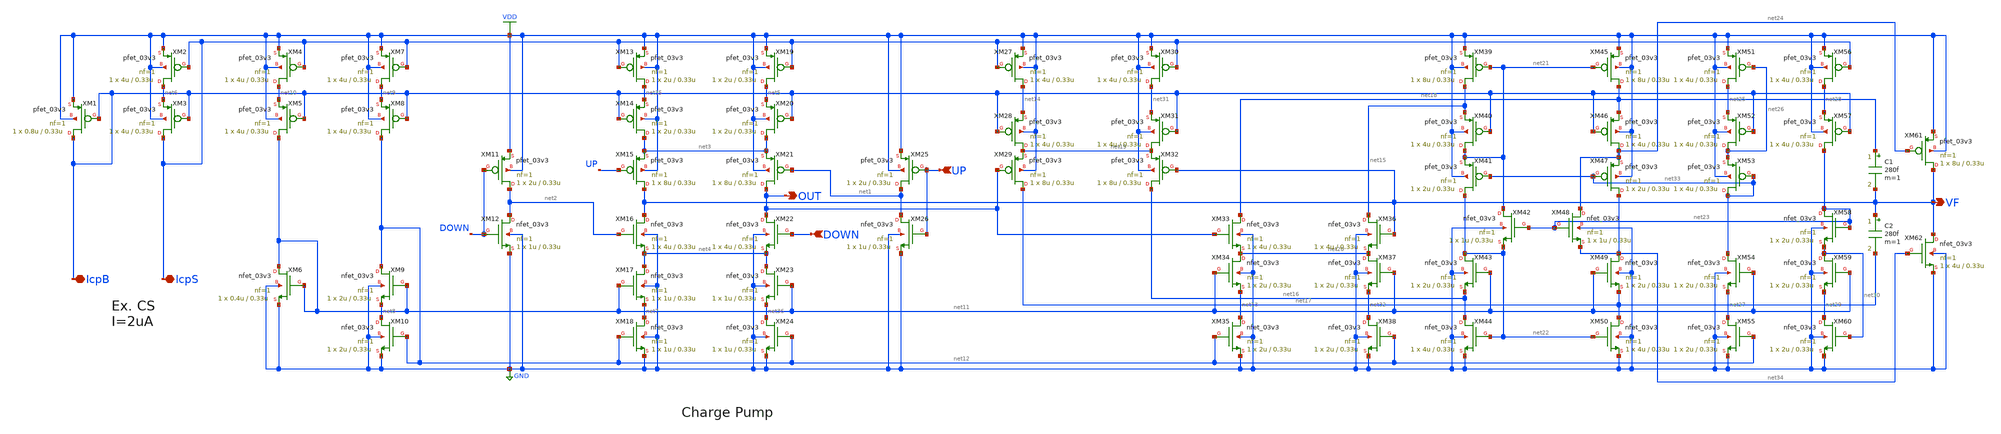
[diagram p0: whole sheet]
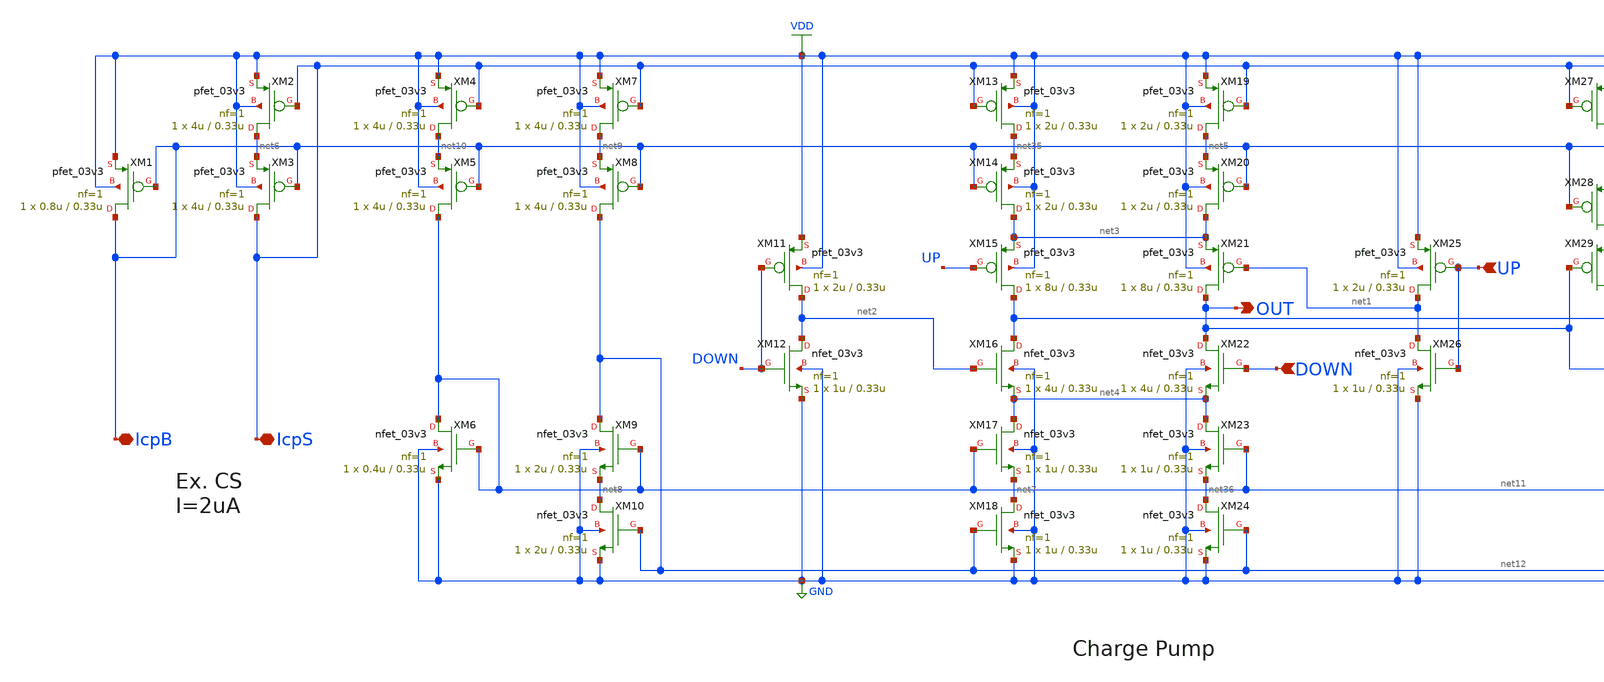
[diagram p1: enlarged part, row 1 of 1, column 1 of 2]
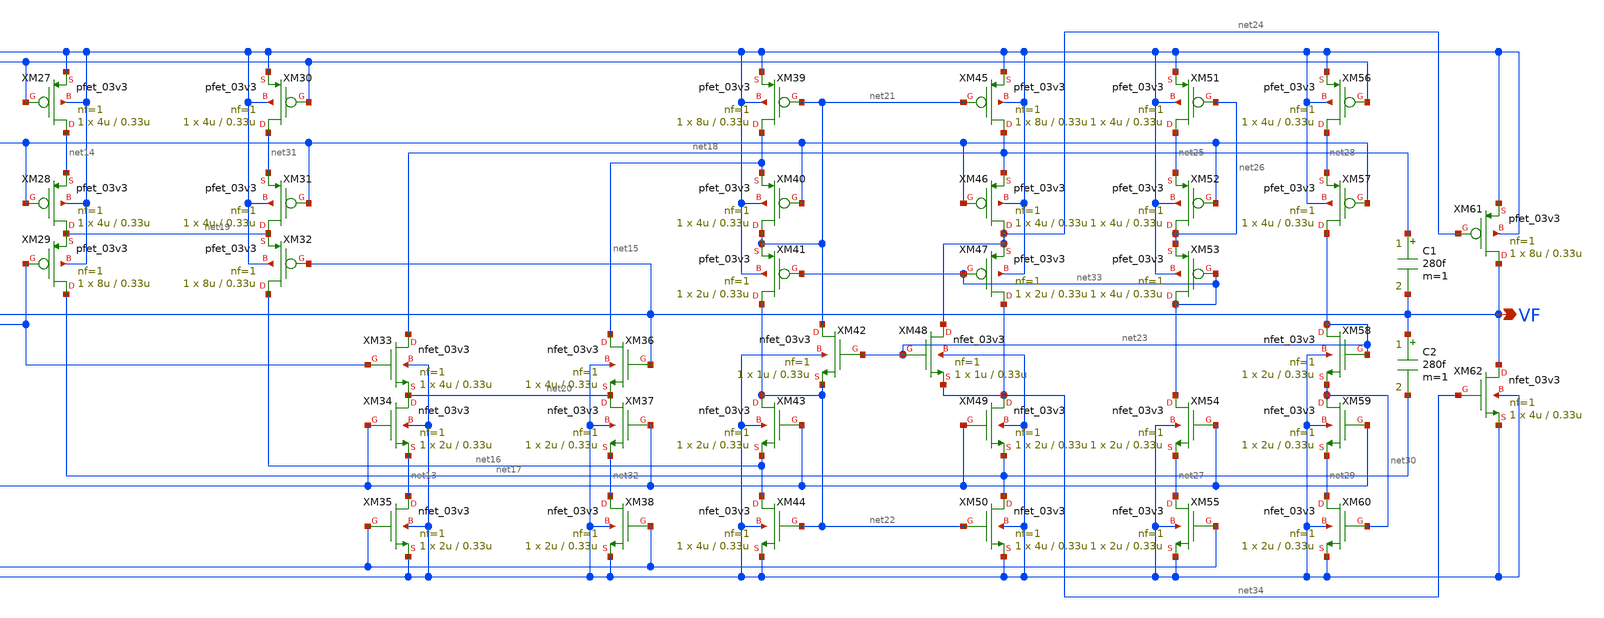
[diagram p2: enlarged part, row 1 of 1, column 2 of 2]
** sch_path: PLL/xschem/cp.sch
**.subckt cp IcpS IcpB DOWN UP OUT VF
*.iopin IcpS
*.iopin IcpB
*.ipin DOWN
*.ipin UP
*.opin OUT
*.opin VF
XM29 net17 OUT net19 VDD pfet_03v3 L=0.33u W=8u nf=1 ad='int((nf+1)/2) * W/nf * 0.18u' as='int((nf+2)/2) * W/nf * 0.18u'
+ pd='2*int((nf+1)/2) * (W/nf + 0.18u)' ps='2*int((nf+2)/2) * (W/nf + 0.18u)' nrd='0.18u / W' nrs='0.18u / W'
+ sa=0 sb=0 sd=0 m=1
XM32 net16 VF net19 VDD pfet_03v3 L=0.33u W=8u nf=1 ad='int((nf+1)/2) * W/nf * 0.18u' as='int((nf+2)/2) * W/nf * 0.18u'
+ pd='2*int((nf+1)/2) * (W/nf + 0.18u)' ps='2*int((nf+2)/2) * (W/nf + 0.18u)' nrd='0.18u / W' nrs='0.18u / W'
+ sa=0 sb=0 sd=0 m=1
XM15 VF UP net3 VDD pfet_03v3 L=0.33u W=8u nf=1 ad='int((nf+1)/2) * W/nf * 0.18u' as='int((nf+2)/2) * W/nf * 0.18u'
+ pd='2*int((nf+1)/2) * (W/nf + 0.18u)' ps='2*int((nf+2)/2) * (W/nf + 0.18u)' nrd='0.18u / W' nrs='0.18u / W'
+ sa=0 sb=0 sd=0 m=1
XM16 VF net2 net4 GND nfet_03v3 L=0.33u W=4u nf=1 ad='int((nf+1)/2) * W/nf * 0.18u' as='int((nf+2)/2) * W/nf * 0.18u'
+ pd='2*int((nf+1)/2) * (W/nf + 0.18u)' ps='2*int((nf+2)/2) * (W/nf + 0.18u)' nrd='0.18u / W' nrs='0.18u / W'
+ sa=0 sb=0 sd=0 m=1
XM11 net2 DOWN VDD VDD pfet_03v3 L=0.33u W=2u nf=1 ad='int((nf+1)/2) * W/nf * 0.18u' as='int((nf+2)/2) * W/nf * 0.18u'
+ pd='2*int((nf+1)/2) * (W/nf + 0.18u)' ps='2*int((nf+2)/2) * (W/nf + 0.18u)' nrd='0.18u / W' nrs='0.18u / W'
+ sa=0 sb=0 sd=0 m=1
XM12 net2 DOWN GND GND nfet_03v3 L=0.33u W=1u nf=1 ad='int((nf+1)/2) * W/nf * 0.18u' as='int((nf+2)/2) * W/nf * 0.18u'
+ pd='2*int((nf+1)/2) * (W/nf + 0.18u)' ps='2*int((nf+2)/2) * (W/nf + 0.18u)' nrd='0.18u / W' nrs='0.18u / W'
+ sa=0 sb=0 sd=0 m=1
XM17 net4 net11 net7 GND nfet_03v3 L=0.33u W=1u nf=1 ad='int((nf+1)/2) * W/nf * 0.18u' as='int((nf+2)/2) * W/nf * 0.18u'
+ pd='2*int((nf+1)/2) * (W/nf + 0.18u)' ps='2*int((nf+2)/2) * (W/nf + 0.18u)' nrd='0.18u / W' nrs='0.18u / W'
+ sa=0 sb=0 sd=0 m=1
XM18 net7 net12 GND GND nfet_03v3 L=0.33u W=1u nf=1 ad='int((nf+1)/2) * W/nf * 0.18u' as='int((nf+2)/2) * W/nf * 0.18u'
+ pd='2*int((nf+1)/2) * (W/nf + 0.18u)' ps='2*int((nf+2)/2) * (W/nf + 0.18u)' nrd='0.18u / W' nrs='0.18u / W'
+ sa=0 sb=0 sd=0 m=1
XM27 net14 IcpS VDD VDD pfet_03v3 L=0.33u W=4u nf=1 ad='int((nf+1)/2) * W/nf * 0.18u' as='int((nf+2)/2) * W/nf * 0.18u'
+ pd='2*int((nf+1)/2) * (W/nf + 0.18u)' ps='2*int((nf+2)/2) * (W/nf + 0.18u)' nrd='0.18u / W' nrs='0.18u / W'
+ sa=0 sb=0 sd=0 m=1
XM28 net19 IcpB net14 VDD pfet_03v3 L=0.33u W=4u nf=1 ad='int((nf+1)/2) * W/nf * 0.18u' as='int((nf+2)/2) * W/nf * 0.18u'
+ pd='2*int((nf+1)/2) * (W/nf + 0.18u)' ps='2*int((nf+2)/2) * (W/nf + 0.18u)' nrd='0.18u / W' nrs='0.18u / W'
+ sa=0 sb=0 sd=0 m=1
XM2 net6 IcpS VDD VDD pfet_03v3 L=0.33u W=4u nf=1 ad='int((nf+1)/2) * W/nf * 0.18u' as='int((nf+2)/2) * W/nf * 0.18u'
+ pd='2*int((nf+1)/2) * (W/nf + 0.18u)' ps='2*int((nf+2)/2) * (W/nf + 0.18u)' nrd='0.18u / W' nrs='0.18u / W'
+ sa=0 sb=0 sd=0 m=1
XM3 IcpS IcpB net6 VDD pfet_03v3 L=0.33u W=4u nf=1 ad='int((nf+1)/2) * W/nf * 0.18u' as='int((nf+2)/2) * W/nf * 0.18u'
+ pd='2*int((nf+1)/2) * (W/nf + 0.18u)' ps='2*int((nf+2)/2) * (W/nf + 0.18u)' nrd='0.18u / W' nrs='0.18u / W'
+ sa=0 sb=0 sd=0 m=1
XM1 IcpB IcpB VDD VDD pfet_03v3 L=0.33u W=0.8u nf=1 ad='int((nf+1)/2) * W/nf * 0.18u' as='int((nf+2)/2) * W/nf * 0.18u'
+ pd='2*int((nf+1)/2) * (W/nf + 0.18u)' ps='2*int((nf+2)/2) * (W/nf + 0.18u)' nrd='0.18u / W' nrs='0.18u / W'
+ sa=0 sb=0 sd=0 m=1
XM9 net12 net11 net8 GND nfet_03v3 L=0.33u W=2u nf=1 ad='int((nf+1)/2) * W/nf * 0.18u' as='int((nf+2)/2) * W/nf * 0.18u'
+ pd='2*int((nf+1)/2) * (W/nf + 0.18u)' ps='2*int((nf+2)/2) * (W/nf + 0.18u)' nrd='0.18u / W' nrs='0.18u / W'
+ sa=0 sb=0 sd=0 m=1
XM10 net8 net12 GND GND nfet_03v3 L=0.33u W=2u nf=1 ad='int((nf+1)/2) * W/nf * 0.18u' as='int((nf+2)/2) * W/nf * 0.18u'
+ pd='2*int((nf+1)/2) * (W/nf + 0.18u)' ps='2*int((nf+2)/2) * (W/nf + 0.18u)' nrd='0.18u / W' nrs='0.18u / W'
+ sa=0 sb=0 sd=0 m=1
XM7 net9 IcpS VDD VDD pfet_03v3 L=0.33u W=4u nf=1 ad='int((nf+1)/2) * W/nf * 0.18u' as='int((nf+2)/2) * W/nf * 0.18u'
+ pd='2*int((nf+1)/2) * (W/nf + 0.18u)' ps='2*int((nf+2)/2) * (W/nf + 0.18u)' nrd='0.18u / W' nrs='0.18u / W'
+ sa=0 sb=0 sd=0 m=1
XM8 net12 IcpB net9 VDD pfet_03v3 L=0.33u W=4u nf=1 ad='int((nf+1)/2) * W/nf * 0.18u' as='int((nf+2)/2) * W/nf * 0.18u'
+ pd='2*int((nf+1)/2) * (W/nf + 0.18u)' ps='2*int((nf+2)/2) * (W/nf + 0.18u)' nrd='0.18u / W' nrs='0.18u / W'
+ sa=0 sb=0 sd=0 m=1
XM4 net10 IcpS VDD VDD pfet_03v3 L=0.33u W=4u nf=1 ad='int((nf+1)/2) * W/nf * 0.18u' as='int((nf+2)/2) * W/nf * 0.18u'
+ pd='2*int((nf+1)/2) * (W/nf + 0.18u)' ps='2*int((nf+2)/2) * (W/nf + 0.18u)' nrd='0.18u / W' nrs='0.18u / W'
+ sa=0 sb=0 sd=0 m=1
XM5 net11 IcpB net10 VDD pfet_03v3 L=0.33u W=4u nf=1 ad='int((nf+1)/2) * W/nf * 0.18u' as='int((nf+2)/2) * W/nf * 0.18u'
+ pd='2*int((nf+1)/2) * (W/nf + 0.18u)' ps='2*int((nf+2)/2) * (W/nf + 0.18u)' nrd='0.18u / W' nrs='0.18u / W'
+ sa=0 sb=0 sd=0 m=1
XM6 net11 net11 GND GND nfet_03v3 L=0.33u W=0.4u nf=1 ad='int((nf+1)/2) * W/nf * 0.18u' as='int((nf+2)/2) * W/nf * 0.18u'
+ pd='2*int((nf+1)/2) * (W/nf + 0.18u)' ps='2*int((nf+2)/2) * (W/nf + 0.18u)' nrd='0.18u / W' nrs='0.18u / W'
+ sa=0 sb=0 sd=0 m=1
XM43 net22 net11 net16 GND nfet_03v3 L=0.33u W=2u nf=1 ad='int((nf+1)/2) * W/nf * 0.18u' as='int((nf+2)/2) * W/nf * 0.18u'
+ pd='2*int((nf+1)/2) * (W/nf + 0.18u)' ps='2*int((nf+2)/2) * (W/nf + 0.18u)' nrd='0.18u / W' nrs='0.18u / W'
+ sa=0 sb=0 sd=0 m=1
XM39 net15 net21 VDD VDD pfet_03v3 L=0.33u W=8u nf=1 ad='int((nf+1)/2) * W/nf * 0.18u' as='int((nf+2)/2) * W/nf * 0.18u'
+ pd='2*int((nf+1)/2) * (W/nf + 0.18u)' ps='2*int((nf+2)/2) * (W/nf + 0.18u)' nrd='0.18u / W' nrs='0.18u / W'
+ sa=0 sb=0 sd=0 m=1
XM44 net16 net22 GND GND nfet_03v3 L=0.33u W=4u nf=1 ad='int((nf+1)/2) * W/nf * 0.18u' as='int((nf+2)/2) * W/nf * 0.18u'
+ pd='2*int((nf+1)/2) * (W/nf + 0.18u)' ps='2*int((nf+2)/2) * (W/nf + 0.18u)' nrd='0.18u / W' nrs='0.18u / W'
+ sa=0 sb=0 sd=0 m=1
XM45 net18 net21 VDD VDD pfet_03v3 L=0.33u W=8u nf=1 ad='int((nf+1)/2) * W/nf * 0.18u' as='int((nf+2)/2) * W/nf * 0.18u'
+ pd='2*int((nf+1)/2) * (W/nf + 0.18u)' ps='2*int((nf+2)/2) * (W/nf + 0.18u)' nrd='0.18u / W' nrs='0.18u / W'
+ sa=0 sb=0 sd=0 m=1
XM46 net24 IcpB net18 VDD pfet_03v3 L=0.33u W=4u nf=1 ad='int((nf+1)/2) * W/nf * 0.18u' as='int((nf+2)/2) * W/nf * 0.18u'
+ pd='2*int((nf+1)/2) * (W/nf + 0.18u)' ps='2*int((nf+2)/2) * (W/nf + 0.18u)' nrd='0.18u / W' nrs='0.18u / W'
+ sa=0 sb=0 sd=0 m=1
XM49 net34 net11 net17 GND nfet_03v3 L=0.33u W=2u nf=1 ad='int((nf+1)/2) * W/nf * 0.18u' as='int((nf+2)/2) * W/nf * 0.18u'
+ pd='2*int((nf+1)/2) * (W/nf + 0.18u)' ps='2*int((nf+2)/2) * (W/nf + 0.18u)' nrd='0.18u / W' nrs='0.18u / W'
+ sa=0 sb=0 sd=0 m=1
XM50 net17 net22 GND GND nfet_03v3 L=0.33u W=4u nf=1 ad='int((nf+1)/2) * W/nf * 0.18u' as='int((nf+2)/2) * W/nf * 0.18u'
+ pd='2*int((nf+1)/2) * (W/nf + 0.18u)' ps='2*int((nf+2)/2) * (W/nf + 0.18u)' nrd='0.18u / W' nrs='0.18u / W'
+ sa=0 sb=0 sd=0 m=1
XM34 net20 net11 net13 GND nfet_03v3 L=0.33u W=2u nf=1 ad='int((nf+1)/2) * W/nf * 0.18u' as='int((nf+2)/2) * W/nf * 0.18u'
+ pd='2*int((nf+1)/2) * (W/nf + 0.18u)' ps='2*int((nf+2)/2) * (W/nf + 0.18u)' nrd='0.18u / W' nrs='0.18u / W'
+ sa=0 sb=0 sd=0 m=1
XM35 net13 net12 GND GND nfet_03v3 L=0.33u W=2u nf=1 ad='int((nf+1)/2) * W/nf * 0.18u' as='int((nf+2)/2) * W/nf * 0.18u'
+ pd='2*int((nf+1)/2) * (W/nf + 0.18u)' ps='2*int((nf+2)/2) * (W/nf + 0.18u)' nrd='0.18u / W' nrs='0.18u / W'
+ sa=0 sb=0 sd=0 m=1
XM33 net18 OUT net20 GND nfet_03v3 L=0.33u W=4u nf=1 ad='int((nf+1)/2) * W/nf * 0.18u' as='int((nf+2)/2) * W/nf * 0.18u'
+ pd='2*int((nf+1)/2) * (W/nf + 0.18u)' ps='2*int((nf+2)/2) * (W/nf + 0.18u)' nrd='0.18u / W' nrs='0.18u / W'
+ sa=0 sb=0 sd=0 m=1
XM36 net15 VF net20 GND nfet_03v3 L=0.33u W=4u nf=1 ad='int((nf+1)/2) * W/nf * 0.18u' as='int((nf+2)/2) * W/nf * 0.18u'
+ pd='2*int((nf+1)/2) * (W/nf + 0.18u)' ps='2*int((nf+2)/2) * (W/nf + 0.18u)' nrd='0.18u / W' nrs='0.18u / W'
+ sa=0 sb=0 sd=0 m=1
XM41 net22 net33 net21 VDD pfet_03v3 L=0.33u W=2u nf=1 ad='int((nf+1)/2) * W/nf * 0.18u' as='int((nf+2)/2) * W/nf * 0.18u'
+ pd='2*int((nf+1)/2) * (W/nf + 0.18u)' ps='2*int((nf+2)/2) * (W/nf + 0.18u)' nrd='0.18u / W' nrs='0.18u / W'
+ sa=0 sb=0 sd=0 m=1
XM42 net21 net23 net22 GND nfet_03v3 L=0.33u W=1u nf=1 ad='int((nf+1)/2) * W/nf * 0.18u' as='int((nf+2)/2) * W/nf * 0.18u'
+ pd='2*int((nf+1)/2) * (W/nf + 0.18u)' ps='2*int((nf+2)/2) * (W/nf + 0.18u)' nrd='0.18u / W' nrs='0.18u / W'
+ sa=0 sb=0 sd=0 m=1
XM47 net34 net33 net24 VDD pfet_03v3 L=0.33u W=2u nf=1 ad='int((nf+1)/2) * W/nf * 0.18u' as='int((nf+2)/2) * W/nf * 0.18u'
+ pd='2*int((nf+1)/2) * (W/nf + 0.18u)' ps='2*int((nf+2)/2) * (W/nf + 0.18u)' nrd='0.18u / W' nrs='0.18u / W'
+ sa=0 sb=0 sd=0 m=1
XM48 net24 net23 net34 GND nfet_03v3 L=0.33u W=1u nf=1 ad='int((nf+1)/2) * W/nf * 0.18u' as='int((nf+2)/2) * W/nf * 0.18u'
+ pd='2*int((nf+1)/2) * (W/nf + 0.18u)' ps='2*int((nf+2)/2) * (W/nf + 0.18u)' nrd='0.18u / W' nrs='0.18u / W'
+ sa=0 sb=0 sd=0 m=1
XM61 VF net24 VDD VDD pfet_03v3 L=0.33u W=8u nf=1 ad='int((nf+1)/2) * W/nf * 0.18u' as='int((nf+2)/2) * W/nf * 0.18u'
+ pd='2*int((nf+1)/2) * (W/nf + 0.18u)' ps='2*int((nf+2)/2) * (W/nf + 0.18u)' nrd='0.18u / W' nrs='0.18u / W'
+ sa=0 sb=0 sd=0 m=1
XM51 net25 net26 VDD VDD pfet_03v3 L=0.33u W=4u nf=1 ad='int((nf+1)/2) * W/nf * 0.18u' as='int((nf+2)/2) * W/nf * 0.18u'
+ pd='2*int((nf+1)/2) * (W/nf + 0.18u)' ps='2*int((nf+2)/2) * (W/nf + 0.18u)' nrd='0.18u / W' nrs='0.18u / W'
+ sa=0 sb=0 sd=0 m=1
XM52 net26 IcpB net25 VDD pfet_03v3 L=0.33u W=4u nf=1 ad='int((nf+1)/2) * W/nf * 0.18u' as='int((nf+2)/2) * W/nf * 0.18u'
+ pd='2*int((nf+1)/2) * (W/nf + 0.18u)' ps='2*int((nf+2)/2) * (W/nf + 0.18u)' nrd='0.18u / W' nrs='0.18u / W'
+ sa=0 sb=0 sd=0 m=1
XM53 net33 net33 net26 VDD pfet_03v3 L=0.33u W=4u nf=1 ad='int((nf+1)/2) * W/nf * 0.18u' as='int((nf+2)/2) * W/nf * 0.18u'
+ pd='2*int((nf+1)/2) * (W/nf + 0.18u)' ps='2*int((nf+2)/2) * (W/nf + 0.18u)' nrd='0.18u / W' nrs='0.18u / W'
+ sa=0 sb=0 sd=0 m=1
XM54 net33 net11 net27 GND nfet_03v3 L=0.33u W=2u nf=1 ad='int((nf+1)/2) * W/nf * 0.18u' as='int((nf+2)/2) * W/nf * 0.18u'
+ pd='2*int((nf+1)/2) * (W/nf + 0.18u)' ps='2*int((nf+2)/2) * (W/nf + 0.18u)' nrd='0.18u / W' nrs='0.18u / W'
+ sa=0 sb=0 sd=0 m=1
XM55 net27 net12 GND GND nfet_03v3 L=0.33u W=2u nf=1 ad='int((nf+1)/2) * W/nf * 0.18u' as='int((nf+2)/2) * W/nf * 0.18u'
+ pd='2*int((nf+1)/2) * (W/nf + 0.18u)' ps='2*int((nf+2)/2) * (W/nf + 0.18u)' nrd='0.18u / W' nrs='0.18u / W'
+ sa=0 sb=0 sd=0 m=1
XM56 net28 IcpS VDD VDD pfet_03v3 L=0.33u W=4u nf=1 ad='int((nf+1)/2) * W/nf * 0.18u' as='int((nf+2)/2) * W/nf * 0.18u'
+ pd='2*int((nf+1)/2) * (W/nf + 0.18u)' ps='2*int((nf+2)/2) * (W/nf + 0.18u)' nrd='0.18u / W' nrs='0.18u / W'
+ sa=0 sb=0 sd=0 m=1
XM57 net23 IcpB net28 VDD pfet_03v3 L=0.33u W=4u nf=1 ad='int((nf+1)/2) * W/nf * 0.18u' as='int((nf+2)/2) * W/nf * 0.18u'
+ pd='2*int((nf+1)/2) * (W/nf + 0.18u)' ps='2*int((nf+2)/2) * (W/nf + 0.18u)' nrd='0.18u / W' nrs='0.18u / W'
+ sa=0 sb=0 sd=0 m=1
XM59 net30 net11 net29 GND nfet_03v3 L=0.33u W=2u nf=1 ad='int((nf+1)/2) * W/nf * 0.18u' as='int((nf+2)/2) * W/nf * 0.18u'
+ pd='2*int((nf+1)/2) * (W/nf + 0.18u)' ps='2*int((nf+2)/2) * (W/nf + 0.18u)' nrd='0.18u / W' nrs='0.18u / W'
+ sa=0 sb=0 sd=0 m=1
XM60 net29 net30 GND GND nfet_03v3 L=0.33u W=2u nf=1 ad='int((nf+1)/2) * W/nf * 0.18u' as='int((nf+2)/2) * W/nf * 0.18u'
+ pd='2*int((nf+1)/2) * (W/nf + 0.18u)' ps='2*int((nf+2)/2) * (W/nf + 0.18u)' nrd='0.18u / W' nrs='0.18u / W'
+ sa=0 sb=0 sd=0 m=1
XM58 net23 net23 net30 GND nfet_03v3 L=0.33u W=2u nf=1 ad='int((nf+1)/2) * W/nf * 0.18u' as='int((nf+2)/2) * W/nf * 0.18u'
+ pd='2*int((nf+1)/2) * (W/nf + 0.18u)' ps='2*int((nf+2)/2) * (W/nf + 0.18u)' nrd='0.18u / W' nrs='0.18u / W'
+ sa=0 sb=0 sd=0 m=1
XM62 VF net34 GND GND nfet_03v3 L=0.33u W=4u nf=1 ad='int((nf+1)/2) * W/nf * 0.18u' as='int((nf+2)/2) * W/nf * 0.18u'
+ pd='2*int((nf+1)/2) * (W/nf + 0.18u)' ps='2*int((nf+2)/2) * (W/nf + 0.18u)' nrd='0.18u / W' nrs='0.18u / W'
+ sa=0 sb=0 sd=0 m=1
XM30 net31 IcpS VDD VDD pfet_03v3 L=0.33u W=4u nf=1 ad='int((nf+1)/2) * W/nf * 0.18u' as='int((nf+2)/2) * W/nf * 0.18u'
+ pd='2*int((nf+1)/2) * (W/nf + 0.18u)' ps='2*int((nf+2)/2) * (W/nf + 0.18u)' nrd='0.18u / W' nrs='0.18u / W'
+ sa=0 sb=0 sd=0 m=1
XM31 net19 IcpB net31 VDD pfet_03v3 L=0.33u W=4u nf=1 ad='int((nf+1)/2) * W/nf * 0.18u' as='int((nf+2)/2) * W/nf * 0.18u'
+ pd='2*int((nf+1)/2) * (W/nf + 0.18u)' ps='2*int((nf+2)/2) * (W/nf + 0.18u)' nrd='0.18u / W' nrs='0.18u / W'
+ sa=0 sb=0 sd=0 m=1
XM37 net20 net11 net32 GND nfet_03v3 L=0.33u W=2u nf=1 ad='int((nf+1)/2) * W/nf * 0.18u' as='int((nf+2)/2) * W/nf * 0.18u'
+ pd='2*int((nf+1)/2) * (W/nf + 0.18u)' ps='2*int((nf+2)/2) * (W/nf + 0.18u)' nrd='0.18u / W' nrs='0.18u / W'
+ sa=0 sb=0 sd=0 m=1
XM38 net32 net12 GND GND nfet_03v3 L=0.33u W=2u nf=1 ad='int((nf+1)/2) * W/nf * 0.18u' as='int((nf+2)/2) * W/nf * 0.18u'
+ pd='2*int((nf+1)/2) * (W/nf + 0.18u)' ps='2*int((nf+2)/2) * (W/nf + 0.18u)' nrd='0.18u / W' nrs='0.18u / W'
+ sa=0 sb=0 sd=0 m=1
C1 net18 VF 280f m=1
C2 VF net17 280f m=1
XM13 net35 IcpS VDD VDD pfet_03v3 L=0.33u W=2u nf=1 ad='int((nf+1)/2) * W/nf * 0.18u' as='int((nf+2)/2) * W/nf * 0.18u'
+ pd='2*int((nf+1)/2) * (W/nf + 0.18u)' ps='2*int((nf+2)/2) * (W/nf + 0.18u)' nrd='0.18u / W' nrs='0.18u / W'
+ sa=0 sb=0 sd=0 m=1
XM14 net3 IcpB net35 VDD pfet_03v3 L=0.33u W=2u nf=1 ad='int((nf+1)/2) * W/nf * 0.18u' as='int((nf+2)/2) * W/nf * 0.18u'
+ pd='2*int((nf+1)/2) * (W/nf + 0.18u)' ps='2*int((nf+2)/2) * (W/nf + 0.18u)' nrd='0.18u / W' nrs='0.18u / W'
+ sa=0 sb=0 sd=0 m=1
XM19 net5 IcpS VDD VDD pfet_03v3 L=0.33u W=2u nf=1 ad='int((nf+1)/2) * W/nf * 0.18u' as='int((nf+2)/2) * W/nf * 0.18u'
+ pd='2*int((nf+1)/2) * (W/nf + 0.18u)' ps='2*int((nf+2)/2) * (W/nf + 0.18u)' nrd='0.18u / W' nrs='0.18u / W'
+ sa=0 sb=0 sd=0 m=1
XM20 net3 IcpB net5 VDD pfet_03v3 L=0.33u W=2u nf=1 ad='int((nf+1)/2) * W/nf * 0.18u' as='int((nf+2)/2) * W/nf * 0.18u'
+ pd='2*int((nf+1)/2) * (W/nf + 0.18u)' ps='2*int((nf+2)/2) * (W/nf + 0.18u)' nrd='0.18u / W' nrs='0.18u / W'
+ sa=0 sb=0 sd=0 m=1
XM21 OUT net1 net3 VDD pfet_03v3 L=0.33u W=8u nf=1 ad='int((nf+1)/2) * W/nf * 0.18u' as='int((nf+2)/2) * W/nf * 0.18u'
+ pd='2*int((nf+1)/2) * (W/nf + 0.18u)' ps='2*int((nf+2)/2) * (W/nf + 0.18u)' nrd='0.18u / W' nrs='0.18u / W'
+ sa=0 sb=0 sd=0 m=1
XM22 OUT DOWN net4 GND nfet_03v3 L=0.33u W=4u nf=1 ad='int((nf+1)/2) * W/nf * 0.18u' as='int((nf+2)/2) * W/nf * 0.18u'
+ pd='2*int((nf+1)/2) * (W/nf + 0.18u)' ps='2*int((nf+2)/2) * (W/nf + 0.18u)' nrd='0.18u / W' nrs='0.18u / W'
+ sa=0 sb=0 sd=0 m=1
XM23 net4 net11 net36 GND nfet_03v3 L=0.33u W=1u nf=1 ad='int((nf+1)/2) * W/nf * 0.18u' as='int((nf+2)/2) * W/nf * 0.18u'
+ pd='2*int((nf+1)/2) * (W/nf + 0.18u)' ps='2*int((nf+2)/2) * (W/nf + 0.18u)' nrd='0.18u / W' nrs='0.18u / W'
+ sa=0 sb=0 sd=0 m=1
XM24 net36 net12 GND GND nfet_03v3 L=0.33u W=1u nf=1 ad='int((nf+1)/2) * W/nf * 0.18u' as='int((nf+2)/2) * W/nf * 0.18u'
+ pd='2*int((nf+1)/2) * (W/nf + 0.18u)' ps='2*int((nf+2)/2) * (W/nf + 0.18u)' nrd='0.18u / W' nrs='0.18u / W'
+ sa=0 sb=0 sd=0 m=1
XM25 net1 UP VDD VDD pfet_03v3 L=0.33u W=2u nf=1 ad='int((nf+1)/2) * W/nf * 0.18u' as='int((nf+2)/2) * W/nf * 0.18u'
+ pd='2*int((nf+1)/2) * (W/nf + 0.18u)' ps='2*int((nf+2)/2) * (W/nf + 0.18u)' nrd='0.18u / W' nrs='0.18u / W'
+ sa=0 sb=0 sd=0 m=1
XM26 net1 UP GND GND nfet_03v3 L=0.33u W=1u nf=1 ad='int((nf+1)/2) * W/nf * 0.18u' as='int((nf+2)/2) * W/nf * 0.18u'
+ pd='2*int((nf+1)/2) * (W/nf + 0.18u)' ps='2*int((nf+2)/2) * (W/nf + 0.18u)' nrd='0.18u / W' nrs='0.18u / W'
+ sa=0 sb=0 sd=0 m=1
XM40 net21 IcpB net15 VDD pfet_03v3 L=0.33u W=4u nf=1 ad='int((nf+1)/2) * W/nf * 0.18u' as='int((nf+2)/2) * W/nf * 0.18u'
+ pd='2*int((nf+1)/2) * (W/nf + 0.18u)' ps='2*int((nf+2)/2) * (W/nf + 0.18u)' nrd='0.18u / W' nrs='0.18u / W'
+ sa=0 sb=0 sd=0 m=1
**.ends
.GLOBAL VDD
.GLOBAL GND
.end
